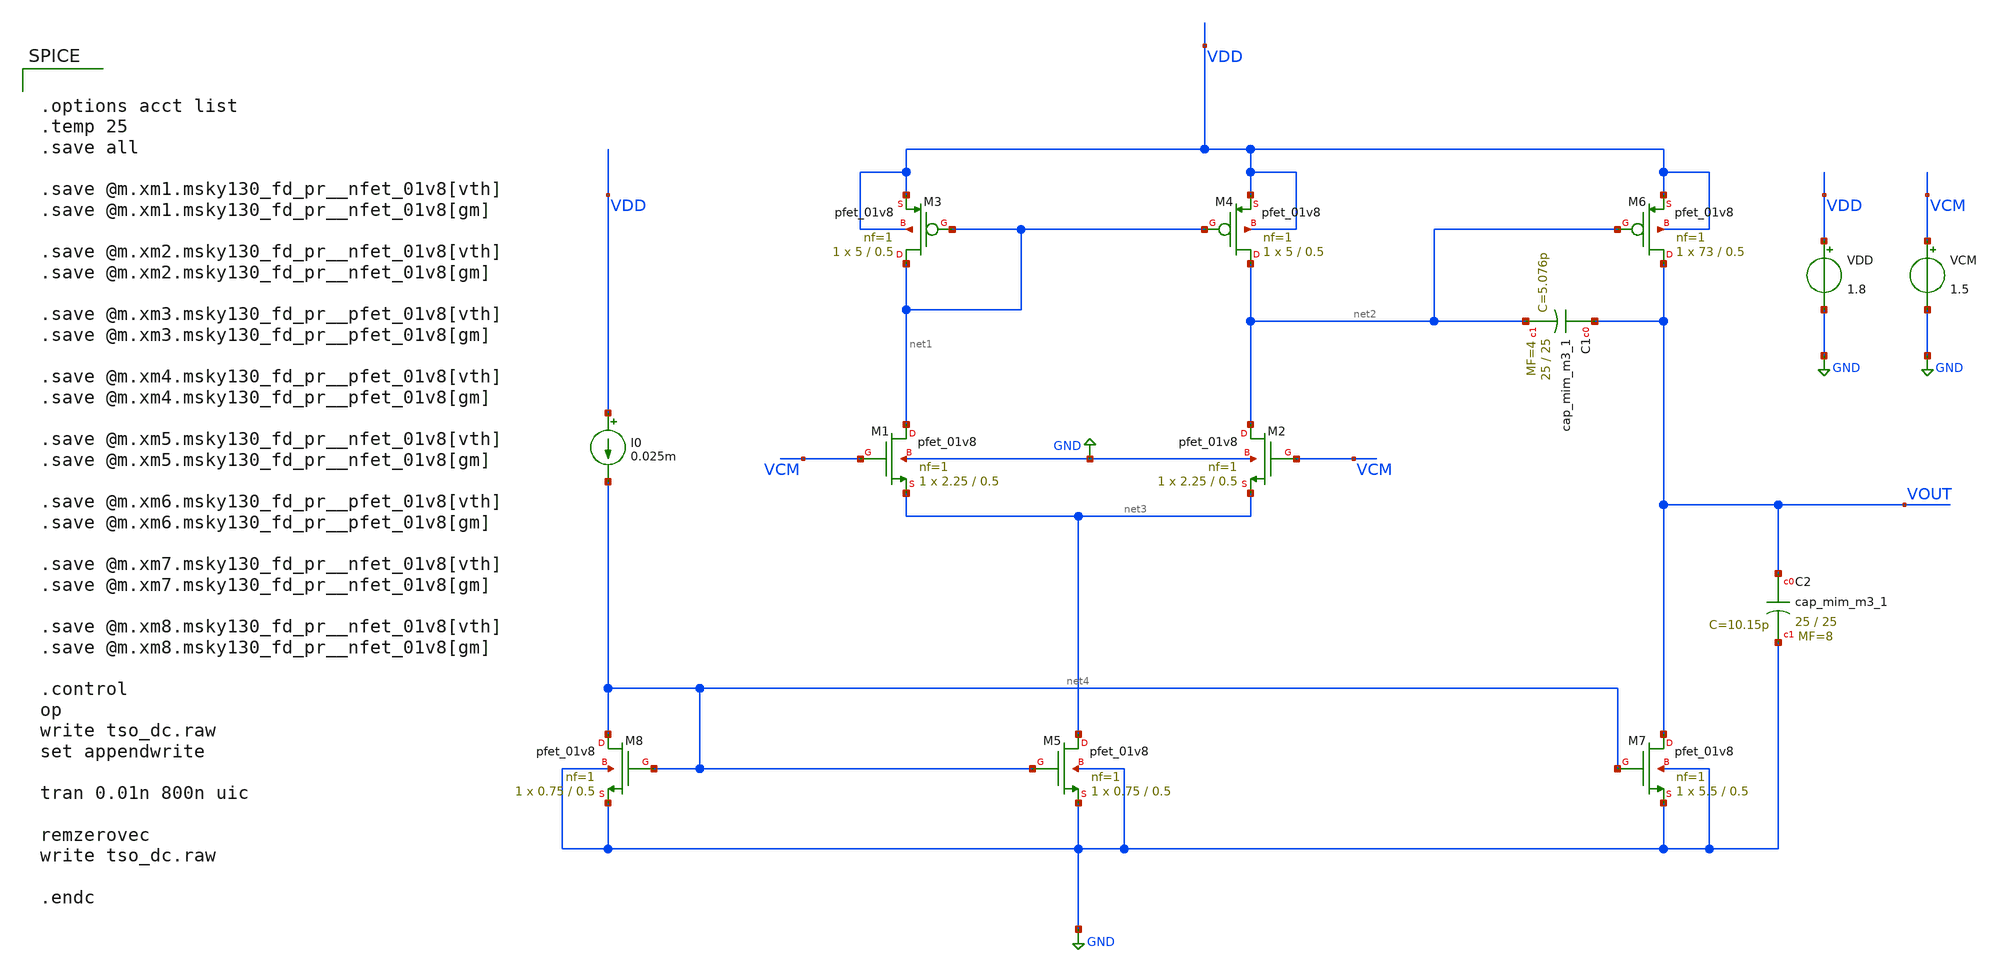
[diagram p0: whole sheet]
** sch_path: xschem/tsopamp.sch
**.subckt tsopamp
XM1 net1 VCM net3 GND sky130_fd_pr__pfet_01v8 L=0.5 W=2.25 nf=1 ad='int((nf+1)/2) * W/nf * 0.29' as='int((nf+2)/2) * W/nf * 0.29'
+ pd='2*int((nf+1)/2) * (W/nf + 0.29)' ps='2*int((nf+2)/2) * (W/nf + 0.29)' nrd='0.29 / W' nrs='0.29 / W'
+ sa=0 sb=0 sd=0 mult=1 m=1
XM2 net2 VCM net3 GND sky130_fd_pr__pfet_01v8 L=0.5 W=2.25 nf=1 ad='int((nf+1)/2) * W/nf * 0.29' as='int((nf+2)/2) * W/nf * 0.29'
+ pd='2*int((nf+1)/2) * (W/nf + 0.29)' ps='2*int((nf+2)/2) * (W/nf + 0.29)' nrd='0.29 / W' nrs='0.29 / W'
+ sa=0 sb=0 sd=0 mult=1 m=1
XM3 net1 net1 VDD VDD sky130_fd_pr__pfet_01v8 L=0.5 W=5 nf=1 ad='int((nf+1)/2) * W/nf * 0.29' as='int((nf+2)/2) * W/nf * 0.29'
+ pd='2*int((nf+1)/2) * (W/nf + 0.29)' ps='2*int((nf+2)/2) * (W/nf + 0.29)' nrd='0.29 / W' nrs='0.29 / W'
+ sa=0 sb=0 sd=0 mult=1 m=1
XM4 net2 net1 VDD VDD sky130_fd_pr__pfet_01v8 L=0.5 W=5 nf=1 ad='int((nf+1)/2) * W/nf * 0.29' as='int((nf+2)/2) * W/nf * 0.29'
+ pd='2*int((nf+1)/2) * (W/nf + 0.29)' ps='2*int((nf+2)/2) * (W/nf + 0.29)' nrd='0.29 / W' nrs='0.29 / W'
+ sa=0 sb=0 sd=0 mult=1 m=1
XM5 net3 net4 GND GND sky130_fd_pr__pfet_01v8 L=0.5 W=0.75 nf=1 ad='int((nf+1)/2) * W/nf * 0.29' as='int((nf+2)/2) * W/nf * 0.29'
+ pd='2*int((nf+1)/2) * (W/nf + 0.29)' ps='2*int((nf+2)/2) * (W/nf + 0.29)' nrd='0.29 / W' nrs='0.29 / W'
+ sa=0 sb=0 sd=0 mult=1 m=1
XM6 VOUT net2 VDD VDD sky130_fd_pr__pfet_01v8 L=0.5 W=73 nf=1 ad='int((nf+1)/2) * W/nf * 0.29' as='int((nf+2)/2) * W/nf * 0.29'
+ pd='2*int((nf+1)/2) * (W/nf + 0.29)' ps='2*int((nf+2)/2) * (W/nf + 0.29)' nrd='0.29 / W' nrs='0.29 / W'
+ sa=0 sb=0 sd=0 mult=1 m=1
XM7 VOUT net4 GND GND sky130_fd_pr__pfet_01v8 L=0.5 W=5.5 nf=1 ad='int((nf+1)/2) * W/nf * 0.29' as='int((nf+2)/2) * W/nf * 0.29'
+ pd='2*int((nf+1)/2) * (W/nf + 0.29)' ps='2*int((nf+2)/2) * (W/nf + 0.29)' nrd='0.29 / W' nrs='0.29 / W'
+ sa=0 sb=0 sd=0 mult=1 m=1
XM8 net4 net4 GND GND sky130_fd_pr__pfet_01v8 L=0.5 W=0.75 nf=1 ad='int((nf+1)/2) * W/nf * 0.29' as='int((nf+2)/2) * W/nf * 0.29'
+ pd='2*int((nf+1)/2) * (W/nf + 0.29)' ps='2*int((nf+2)/2) * (W/nf + 0.29)' nrd='0.29 / W' nrs='0.29 / W'
+ sa=0 sb=0 sd=0 mult=1 m=1
XC1 VOUT net2 sky130_fd_pr__cap_mim_m3_1 W=25 L=25 MF=4 m=4
XC2 VOUT GND sky130_fd_pr__cap_mim_m3_1 W=25 L=25 MF=8 m=8
I0 VDD net4 0.025m
VDD VDD GND 1.8
VCM VCM GND 1.5
**** begin user architecture code


.options acct list
.temp 25
.save all

.save @m.xm1.msky130_fd_pr__nfet_01v8[vth]
.save @m.xm1.msky130_fd_pr__nfet_01v8[gm]

.save @m.xm2.msky130_fd_pr__nfet_01v8[vth]
.save @m.xm2.msky130_fd_pr__nfet_01v8[gm]

.save @m.xm3.msky130_fd_pr__pfet_01v8[vth]
.save @m.xm3.msky130_fd_pr__pfet_01v8[gm]

.save @m.xm4.msky130_fd_pr__pfet_01v8[vth]
.save @m.xm4.msky130_fd_pr__pfet_01v8[gm]

.save @m.xm5.msky130_fd_pr__nfet_01v8[vth]
.save @m.xm5.msky130_fd_pr__nfet_01v8[gm]

.save @m.xm6.msky130_fd_pr__pfet_01v8[vth]
.save @m.xm6.msky130_fd_pr__pfet_01v8[gm]

.save @m.xm7.msky130_fd_pr__nfet_01v8[vth]
.save @m.xm7.msky130_fd_pr__nfet_01v8[gm]

.save @m.xm8.msky130_fd_pr__nfet_01v8[vth]
.save @m.xm8.msky130_fd_pr__nfet_01v8[gm]

.control
op
write tso_dc.raw
set appendwrite

tran 0.01n 800n uic

remzerovec
write tso_dc.raw

.endc




** opencircuitdesign pdks install
.lib $::SKYWATER_MODELS/sky130.lib.spice tt


**** end user architecture code
**.ends
.GLOBAL GND
.end
